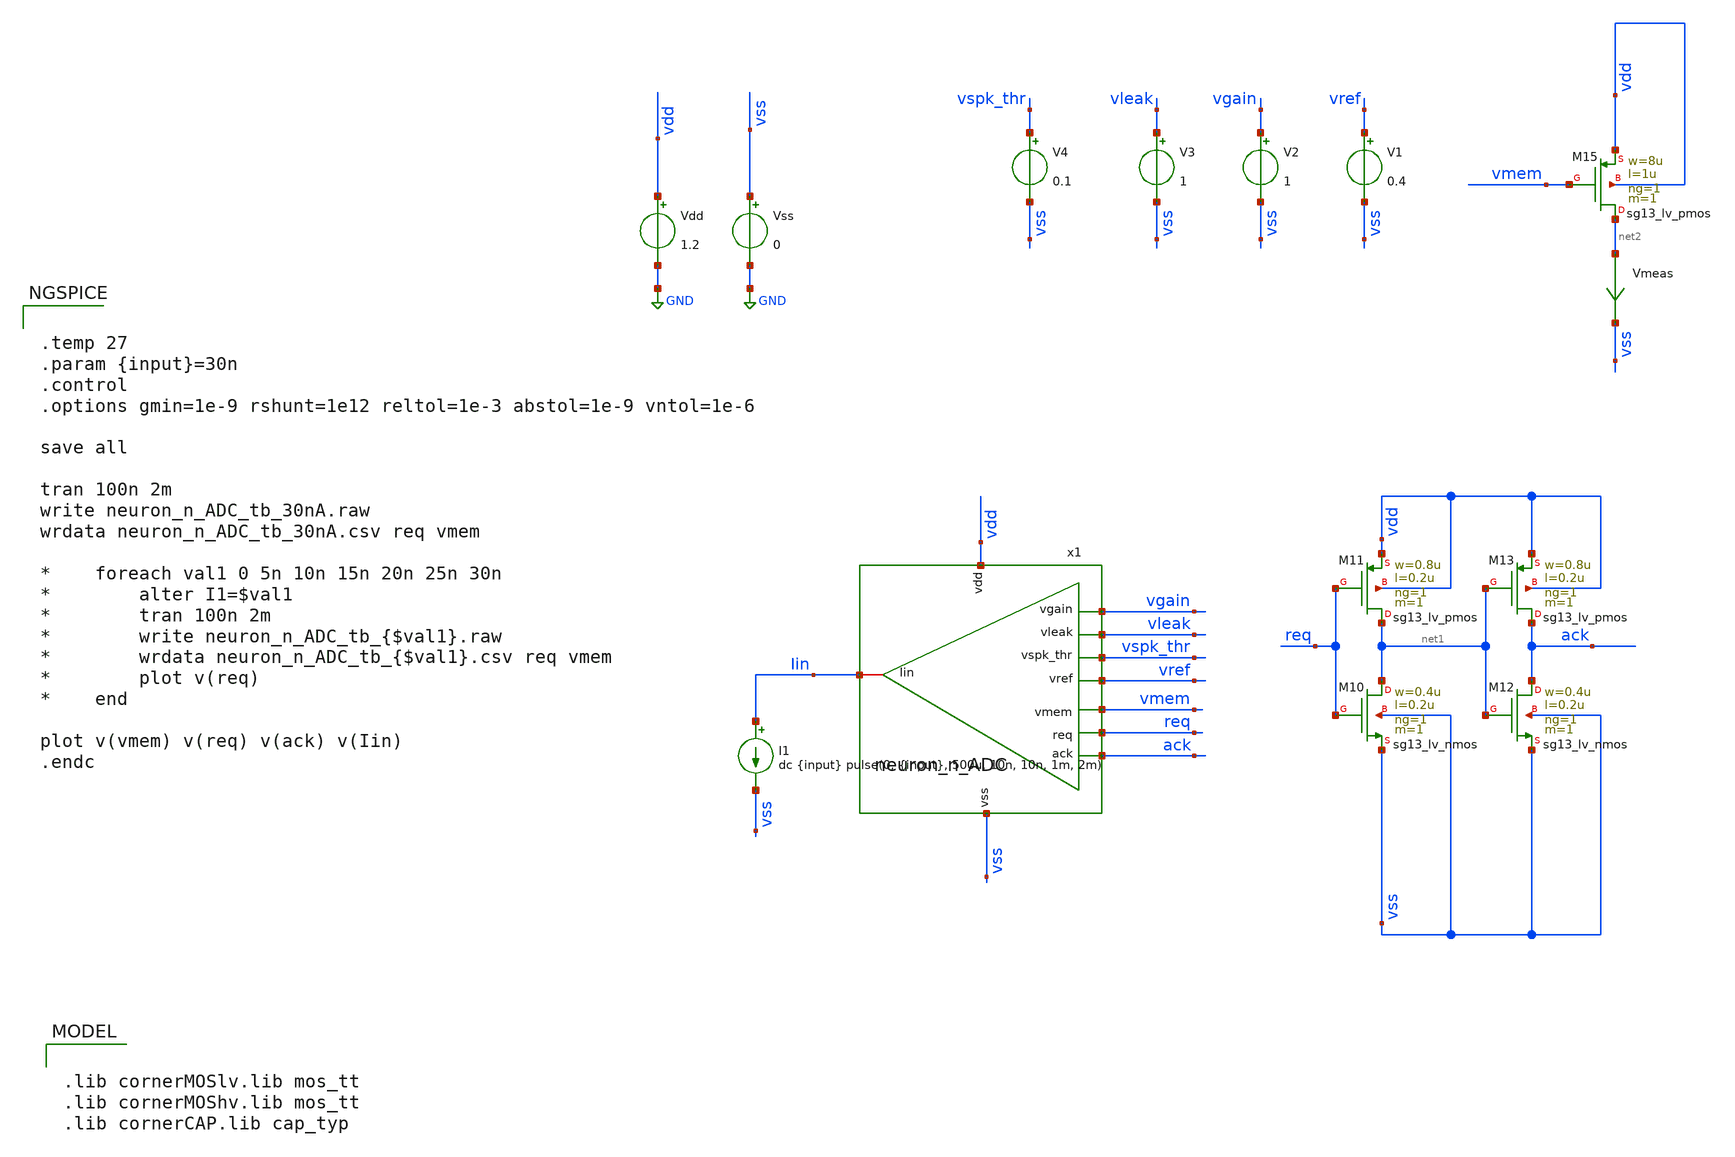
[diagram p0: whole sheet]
** sch_path: v2_feature_extr_withf/neuron_n_ADC_tb.sch
* (c) 2024-2025 Harald Pretl, Apache-2.0 license
**.subckt neuron_n_ADC_tb
XM10 net1 req vss vss sg13_lv_nmos w=0.4u l=0.2u ng=1 m=1 mm_ok=1
XM11 net1 req vdd vdd sg13_lv_pmos w=0.8u l=0.2u ng=1 m=1 mm_ok=1
XM12 ack net1 vss vss sg13_lv_nmos w=0.4u l=0.2u ng=1 m=1 mm_ok=1
XM13 ack net1 vdd vdd sg13_lv_pmos w=0.8u l=0.2u ng=1 m=1 mm_ok=1
Vdd vdd GND 1.2
Vss vss GND 0
I1 Iin vss dc {input} pulse(0, {input}, 500u, 10n, 10n, 1m, 2m)
XM15 net2 vmem vdd vdd sg13_lv_pmos w=8u l=1u ng=1 m=1 mm_ok=1
Vmeas net2 vss 0
.save i(vmeas)
V1 vref vss 0.4
x1 vdd vgain req ack vmem vspk_thr Iin vref vss vleak neuron_n_ADC
V2 vgain vss 1
V3 vleak vss 1
V4 vspk_thr vss 0.1
**** begin user architecture code


.temp 27
.param {input}=30n
.control
.options gmin=1e-9 rshunt=1e12 reltol=1e-3 abstol=1e-9 vntol=1e-6

save all

tran 100n 2m
write neuron_n_ADC_tb_30nA.raw
wrdata neuron_n_ADC_tb_30nA.csv req vmem

*    foreach val1 0 5n 10n 15n 20n 25n 30n
*        alter I1=$val1
*        tran 100n 2m
*        write neuron_n_ADC_tb_{$val1}.raw
*        wrdata neuron_n_ADC_tb_{$val1}.csv req vmem
*        plot v(req)
*    end

plot v(vmem) v(req) v(ack) v(Iin)
.endc



.lib cornerMOSlv.lib mos_tt
.lib cornerMOShv.lib mos_tt
.lib cornerCAP.lib cap_typ

**** end user architecture code
**.ends
.GLOBAL GND
.end
